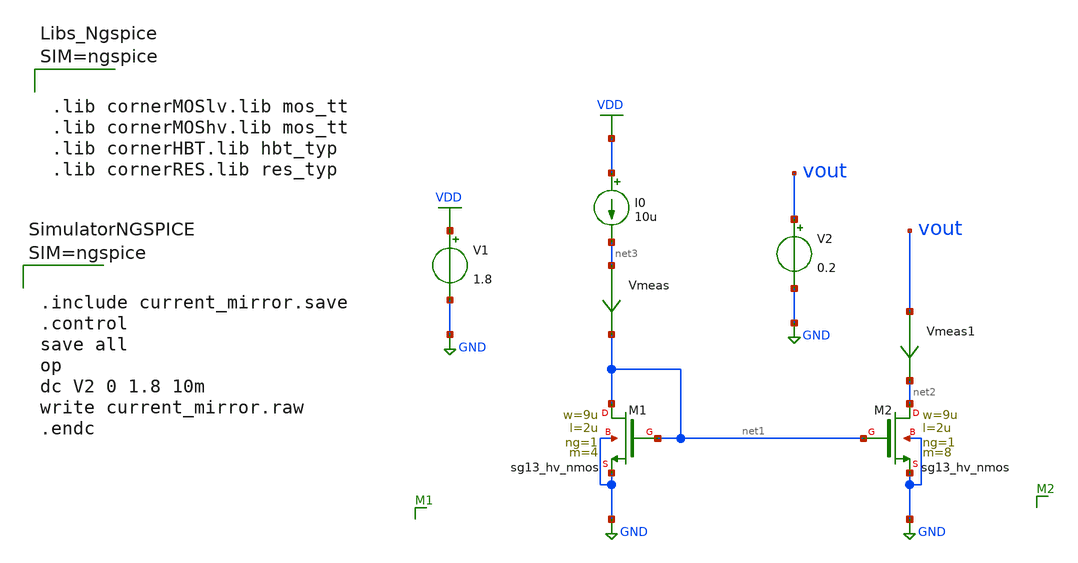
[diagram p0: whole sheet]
** sch_path: Schematics/lab_4/current_mirror.sch
**.subckt current_mirror
I0 VDD net3 10u
V1 VDD GND 1.8
XM1 net1 net1 GND GND sg13_hv_nmos w=9u l=2u ng=1 m=4 mm_ok=1
XM2 net2 net1 GND GND sg13_hv_nmos w=9u l=2u ng=1 m=8 mm_ok=1
Vmeas net3 net1 0
.save i(vmeas)
V2 vout GND 0.2
Vmeas1 vout net2 0
.save i(vmeas1)
**** begin user architecture code



.lib cornerMOSlv.lib mos_tt
.lib cornerMOShv.lib mos_tt
.lib cornerHBT.lib hbt_typ
.lib cornerRES.lib res_typ






.include current_mirror.save
.control
save all
op
dc V2 0 1.8 10m
write current_mirror.raw
.endc



**** end user architecture code
**.ends
.GLOBAL VDD
.GLOBAL GND
.end
